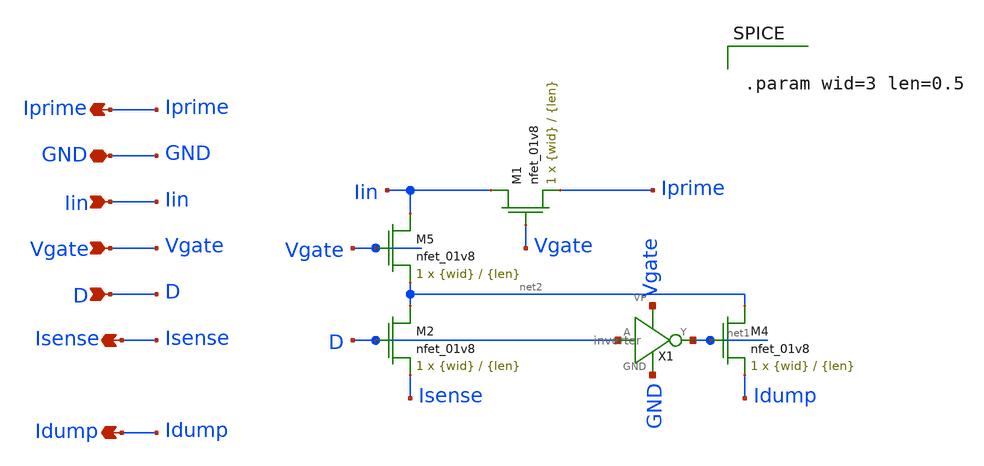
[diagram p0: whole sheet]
** sch_path: final/LDS/daccell_LDS.sch
**.subckt daccell_LDS GND Isense Idump Iin Iprime Vgate D
*.iopin GND
*.opin Isense
*.opin Idump
*.ipin Iin
*.opin Iprime
*.ipin Vgate
*.ipin D
XM5 Iin Vgate net2 GND sky130_fd_pr__nfet_01v8 L={len} W={wid} nf=1 ad='int((nf+1)/2) * W/nf * 0.29'
+ as='int((nf+2)/2) * W/nf * 0.29' pd='2*int((nf+1)/2) * (W/nf + 0.29)' ps='2*int((nf+2)/2) * (W/nf + 0.29)'
+ nrd='0.29 / W' nrs='0.29 / W' sa=0 sb=0 sd=0 mult=1 m=1
XM2 net2 D Isense GND sky130_fd_pr__nfet_01v8 L={len} W={wid} nf=1 ad='int((nf+1)/2) * W/nf * 0.29' as='int((nf+2)/2) * W/nf * 0.29'
+ pd='2*int((nf+1)/2) * (W/nf + 0.29)' ps='2*int((nf+2)/2) * (W/nf + 0.29)' nrd='0.29 / W' nrs='0.29 / W'
+ sa=0 sb=0 sd=0 mult=1 m=1
XM4 net2 net1 Idump GND sky130_fd_pr__nfet_01v8 L={len} W={wid} nf=1 ad='int((nf+1)/2) * W/nf * 0.29'
+ as='int((nf+2)/2) * W/nf * 0.29' pd='2*int((nf+1)/2) * (W/nf + 0.29)' ps='2*int((nf+2)/2) * (W/nf + 0.29)'
+ nrd='0.29 / W' nrs='0.29 / W' sa=0 sb=0 sd=0 mult=1 m=1
XM1 Iin Vgate Iprime GND sky130_fd_pr__nfet_01v8 L={len} W={wid} nf=1 ad='int((nf+1)/2) * W/nf * 0.29'
+ as='int((nf+2)/2) * W/nf * 0.29' pd='2*int((nf+1)/2) * (W/nf + 0.29)' ps='2*int((nf+2)/2) * (W/nf + 0.29)'
+ nrd='0.29 / W' nrs='0.29 / W' sa=0 sb=0 sd=0 mult=1 m=1
X1 Vgate D net1 GND inverter
**** begin user architecture code


.param wid=3 len=0.5


**** end user architecture code
**.ends

* expanding   symbol:  inverter.sym # of pins=4
** sym_path: final/LDS/inverter.sym
** sch_path: final/LDS/inverter.sch
.subckt inverter VP A Y GND
*.ipin A
*.iopin VP
*.iopin GND
*.opin Y
**** begin user architecture code


.param wid=3 len=0.5


**** end user architecture code
XM1 Y A VP VDD sky130_fd_pr__pfet_01v8 L={len} W={wid} nf=1 ad='int((nf+1)/2) * W/nf * 0.29' as='int((nf+2)/2) * W/nf * 0.29'
+ pd='2*int((nf+1)/2) * (W/nf + 0.29)' ps='2*int((nf+2)/2) * (W/nf + 0.29)' nrd='0.29 / W' nrs='0.29 / W'
+ sa=0 sb=0 sd=0 mult=1 m=1
XM2 Y A GND GND sky130_fd_pr__nfet_01v8 L={len} W={wid} nf=1 ad='int((nf+1)/2) * W/nf * 0.29' as='int((nf+2)/2) * W/nf * 0.29'
+ pd='2*int((nf+1)/2) * (W/nf + 0.29)' ps='2*int((nf+2)/2) * (W/nf + 0.29)' nrd='0.29 / W' nrs='0.29 / W'
+ sa=0 sb=0 sd=0 mult=1 m=1
.ends

.end
